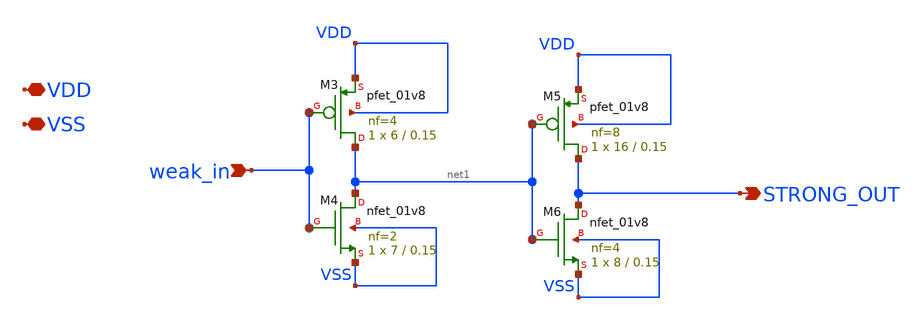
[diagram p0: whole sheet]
** sch_path: xschem/tuning/inverter_buffer_tune.sch
**.subckt inverter_buffer_tune VDD VSS weak_in STRONG_OUT
*.iopin VDD
*.iopin VSS
*.ipin weak_in
*.opin STRONG_OUT
XM3 net1 weak_in VDD VDD sky130_fd_pr__pfet_01v8 L=0.15 W=6 nf=4 ad='int((nf+1)/2) * W/nf * 0.29' as='int((nf+2)/2) * W/nf * 0.29'
+ pd='2*int((nf+1)/2) * (W/nf + 0.29)' ps='2*int((nf+2)/2) * (W/nf + 0.29)' nrd='0.29 / W' nrs='0.29 / W'
+ sa=0 sb=0 sd=0 mult=1 m=1
XM4 net1 weak_in VSS VSS sky130_fd_pr__nfet_01v8 L=0.15 W=7 nf=2 ad='int((nf+1)/2) * W/nf * 0.29' as='int((nf+2)/2) * W/nf * 0.29'
+ pd='2*int((nf+1)/2) * (W/nf + 0.29)' ps='2*int((nf+2)/2) * (W/nf + 0.29)' nrd='0.29 / W' nrs='0.29 / W'
+ sa=0 sb=0 sd=0 mult=1 m=1
XM5 STRONG_OUT net1 VDD VDD sky130_fd_pr__pfet_01v8 L=0.15 W=16 nf=8 ad='int((nf+1)/2) * W/nf * 0.29'
+ as='int((nf+2)/2) * W/nf * 0.29' pd='2*int((nf+1)/2) * (W/nf + 0.29)' ps='2*int((nf+2)/2) * (W/nf + 0.29)'
+ nrd='0.29 / W' nrs='0.29 / W' sa=0 sb=0 sd=0 mult=1 m=1
XM6 STRONG_OUT net1 VSS VSS sky130_fd_pr__nfet_01v8 L=0.15 W=8 nf=4 ad='int((nf+1)/2) * W/nf * 0.29'
+ as='int((nf+2)/2) * W/nf * 0.29' pd='2*int((nf+1)/2) * (W/nf + 0.29)' ps='2*int((nf+2)/2) * (W/nf + 0.29)'
+ nrd='0.29 / W' nrs='0.29 / W' sa=0 sb=0 sd=0 mult=1 m=1
**.ends
.end
